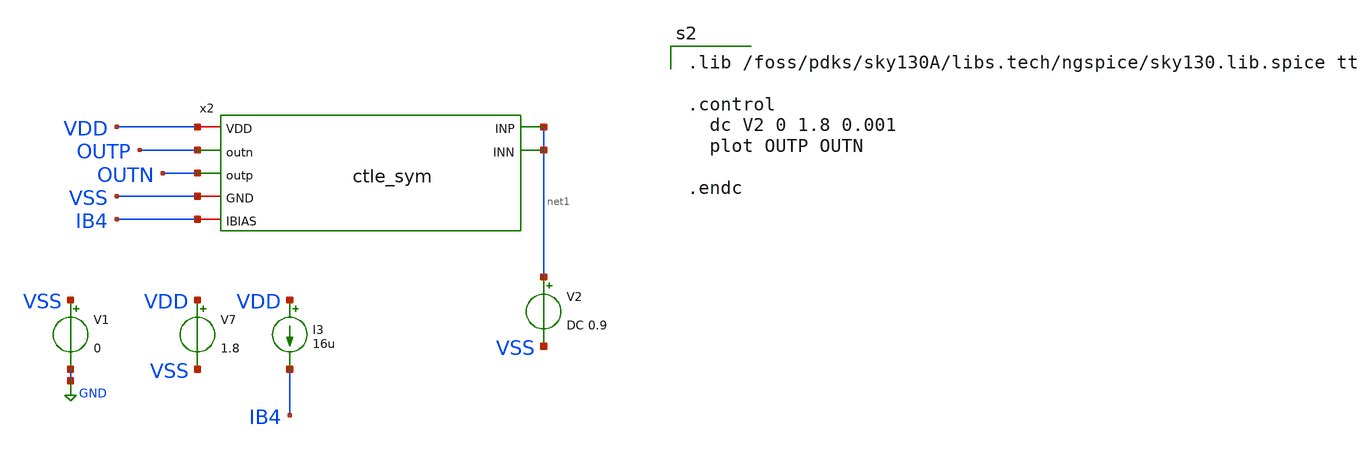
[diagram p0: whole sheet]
** sch_path: pd-converter/ctle-icmr.sch
**.subckt ctle-icmr
x2 VDD OUTP OUTN net1 net1 VSS IB4 ctle_sym
V1 VSS GND 0
V2 net1 VSS DC 0.9
V7 VDD VSS 1.8
I3 VDD IB4 16u
**** begin user architecture code

.lib /foss/pdks/sky130A/libs.tech/ngspice/sky130.lib.spice tt

.control
  dc V2 0 1.8 0.001
  plot OUTP OUTN

.endc


**** end user architecture code
**.ends

* expanding   symbol:  /foss/designs/afe-icdec-teknofest-2026/CTLE/ctle_sym.sym # of pins=7
** sym_path: CTLE/ctle_sym.sym
** sch_path: CTLE/ctle_sym.sch
.subckt ctle_sym VDD outn outp INP INN GND IBIAS
*.opin outp
*.opin outn
*.ipin INN
*.iopin VDD
*.iopin GND
*.iopin IBIAS
*.ipin INP
XM1 outp INP net1 GND sky130_fd_pr__nfet_01v8_lvt L=0.15 W=2 nf=1 ad='int((nf+1)/2) * W/nf * 0.29' as='int((nf+2)/2) * W/nf * 0.29'
+ pd='2*int((nf+1)/2) * (W/nf + 0.29)' ps='2*int((nf+2)/2) * (W/nf + 0.29)' nrd='0.29 / W' nrs='0.29 / W'
+ sa=0 sb=0 sd=0 mult=15 m=15
XM2 outn INN net2 GND sky130_fd_pr__nfet_01v8_lvt L=0.15 W=2 nf=1 ad='int((nf+1)/2) * W/nf * 0.29' as='int((nf+2)/2) * W/nf * 0.29'
+ pd='2*int((nf+1)/2) * (W/nf + 0.29)' ps='2*int((nf+2)/2) * (W/nf + 0.29)' nrd='0.29 / W' nrs='0.29 / W'
+ sa=0 sb=0 sd=0 mult=15 m=15
XM3 net1 IBIAS GND GND sky130_fd_pr__nfet_01v8_lvt L=1 W=2 nf=1 ad='int((nf+1)/2) * W/nf * 0.29' as='int((nf+2)/2) * W/nf * 0.29'
+ pd='2*int((nf+1)/2) * (W/nf + 0.29)' ps='2*int((nf+2)/2) * (W/nf + 0.29)' nrd='0.29 / W' nrs='0.29 / W'
+ sa=0 sb=0 sd=0 mult=24 m=24
XM4 net2 IBIAS GND GND sky130_fd_pr__nfet_01v8_lvt L=1 W=2 nf=1 ad='int((nf+1)/2) * W/nf * 0.29' as='int((nf+2)/2) * W/nf * 0.29'
+ pd='2*int((nf+1)/2) * (W/nf + 0.29)' ps='2*int((nf+2)/2) * (W/nf + 0.29)' nrd='0.29 / W' nrs='0.29 / W'
+ sa=0 sb=0 sd=0 mult=24 m=24
XM5 IBIAS IBIAS GND GND sky130_fd_pr__nfet_01v8_lvt L=1 W=2 nf=1 ad='int((nf+1)/2) * W/nf * 0.29' as='int((nf+2)/2) * W/nf * 0.29'
+ pd='2*int((nf+1)/2) * (W/nf + 0.29)' ps='2*int((nf+2)/2) * (W/nf + 0.29)' nrd='0.29 / W' nrs='0.29 / W'
+ sa=0 sb=0 sd=0 mult=1 m=1
RD1 VDD outp 280 m=1
RD2 VDD outn 280 m=1
CS net1 net2 134f m=1
RS net1 net2 1400 m=1
C1 outp GND 20f m=1
C2 outn GND 20f m=1
.ends

.GLOBAL GND
.end
